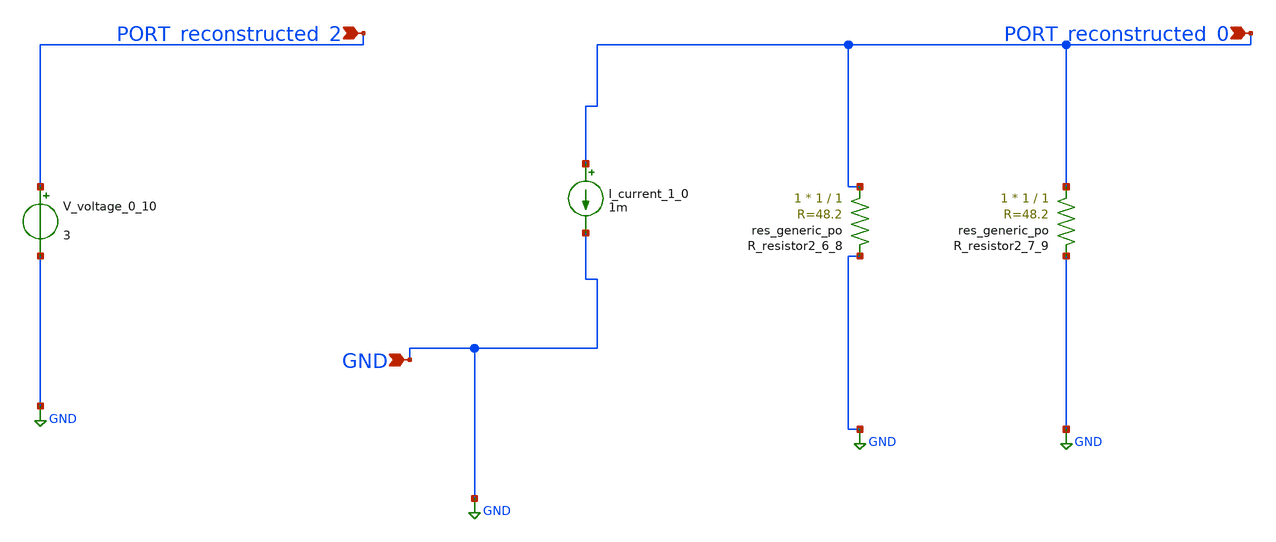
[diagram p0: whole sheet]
** sch_path: schematics/AMSNet/68.sch
**.subckt 68 PORT_reconstructed_2 PORT_reconstructed_0 GND
*.ipin PORT_reconstructed_2
*.ipin PORT_reconstructed_0
*.ipin GND
I_current_1_0 PORT_reconstructed_0 GND 1m
XR_resistor2_6_8 PORT_reconstructed_0 GND sky130_fd_pr__res_generic_po W=1 L=1 m=1
XR_resistor2_7_9 PORT_reconstructed_0 GND sky130_fd_pr__res_generic_po W=1 L=1 m=1
V_voltage_0_10 PORT_reconstructed_2 GND 3
**.ends
.GLOBAL GND
.end
